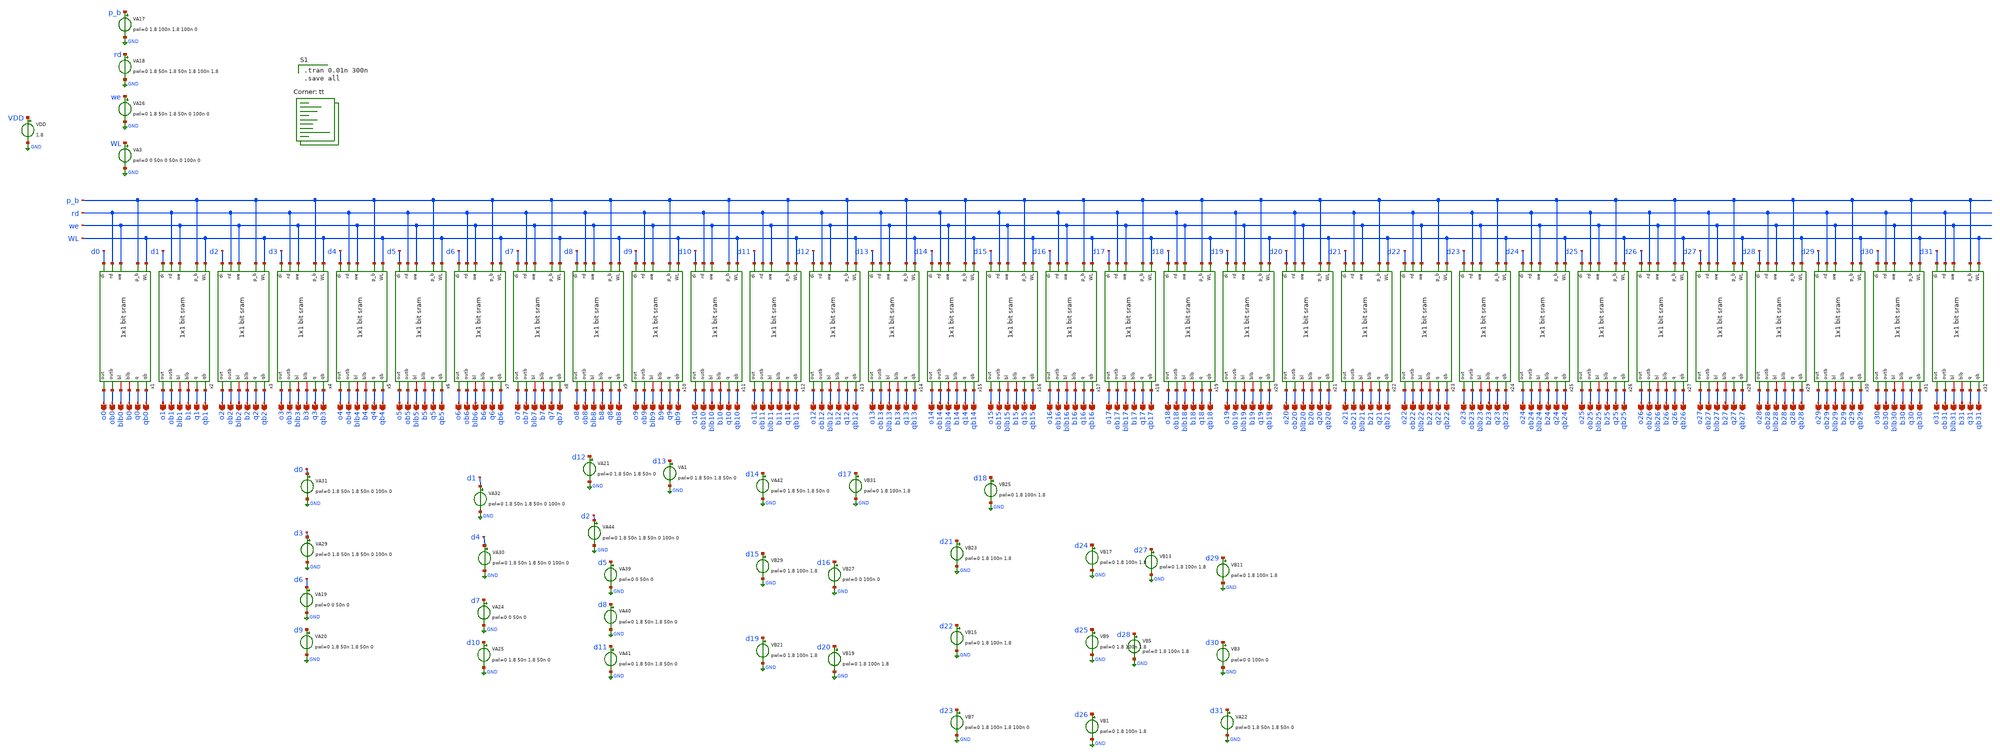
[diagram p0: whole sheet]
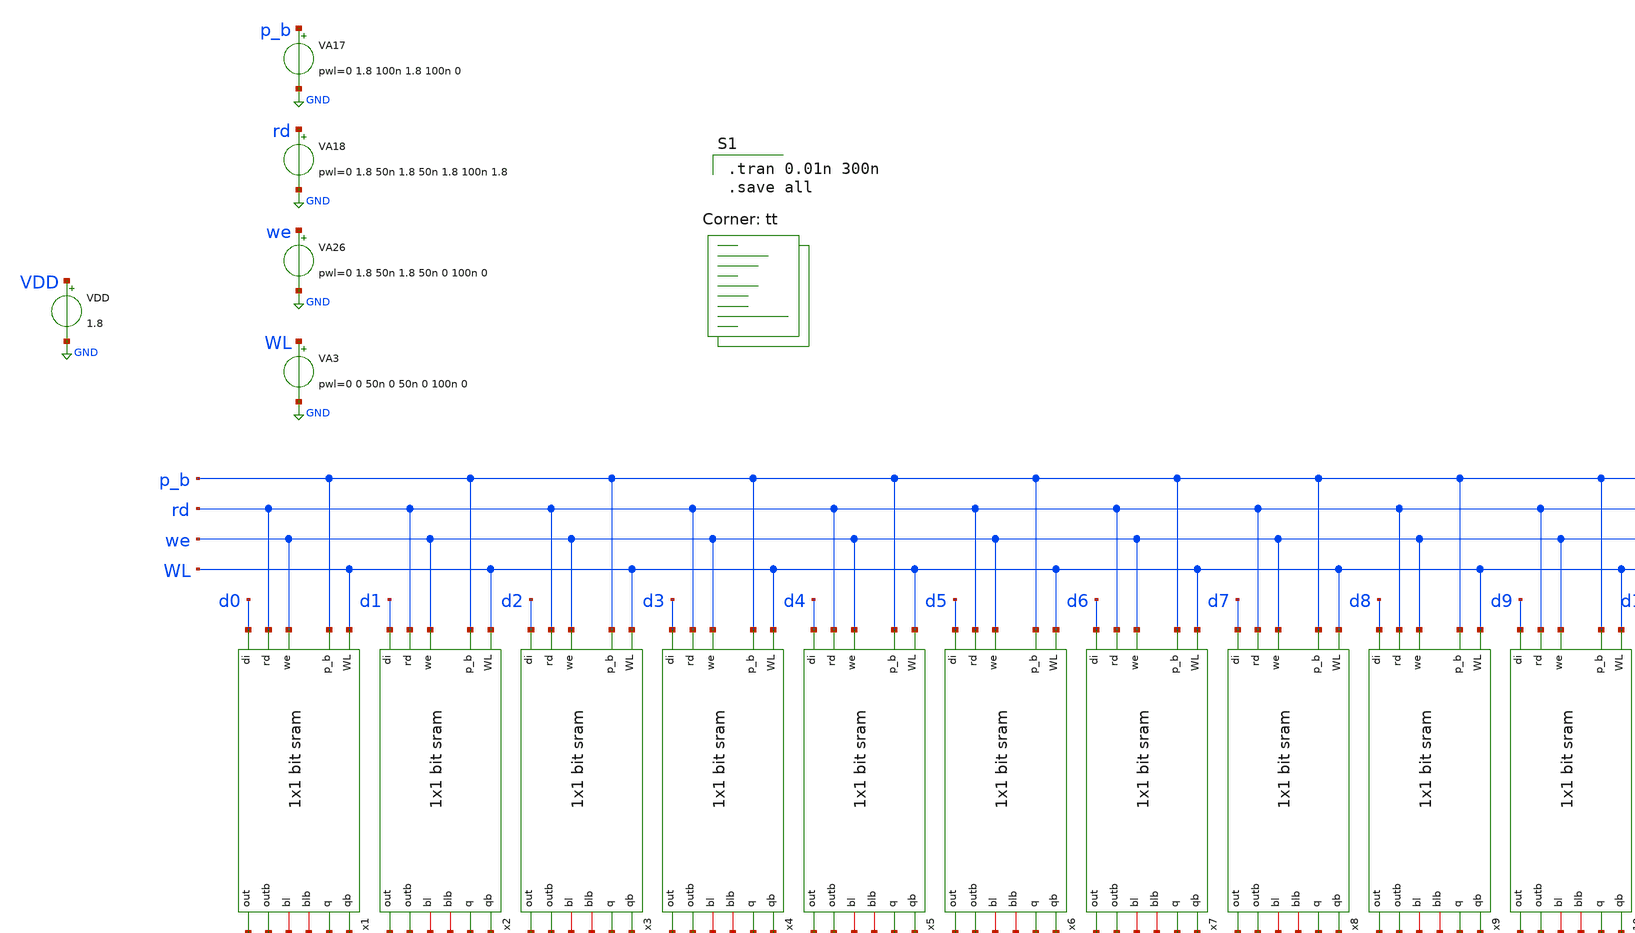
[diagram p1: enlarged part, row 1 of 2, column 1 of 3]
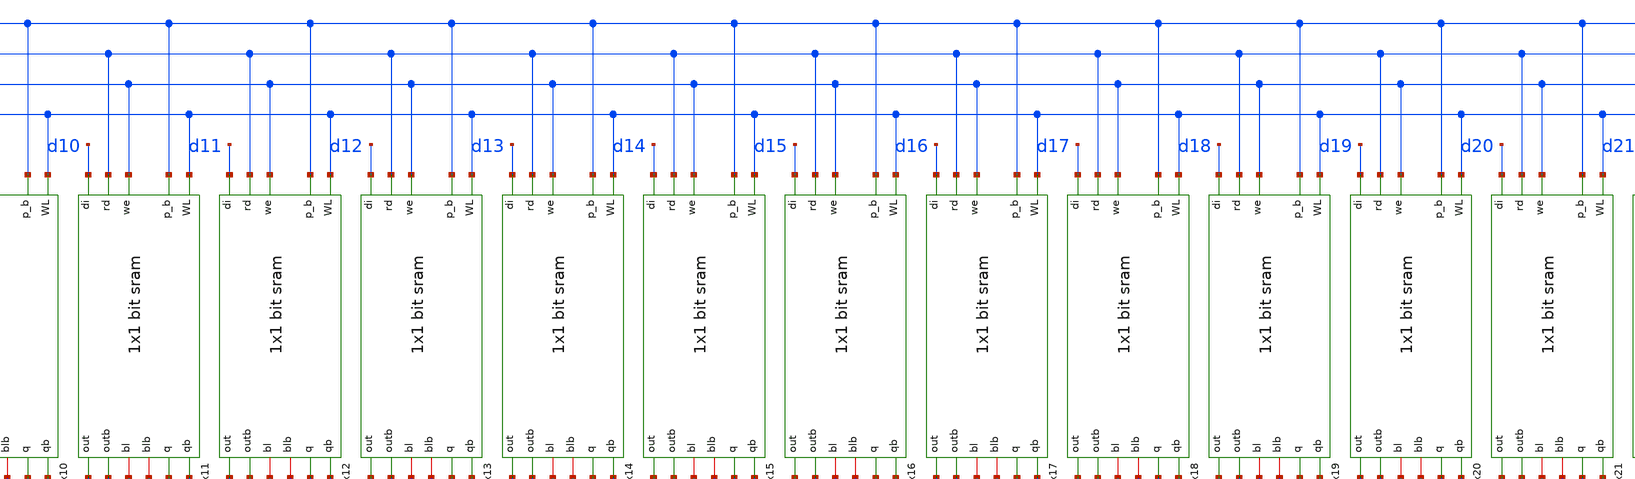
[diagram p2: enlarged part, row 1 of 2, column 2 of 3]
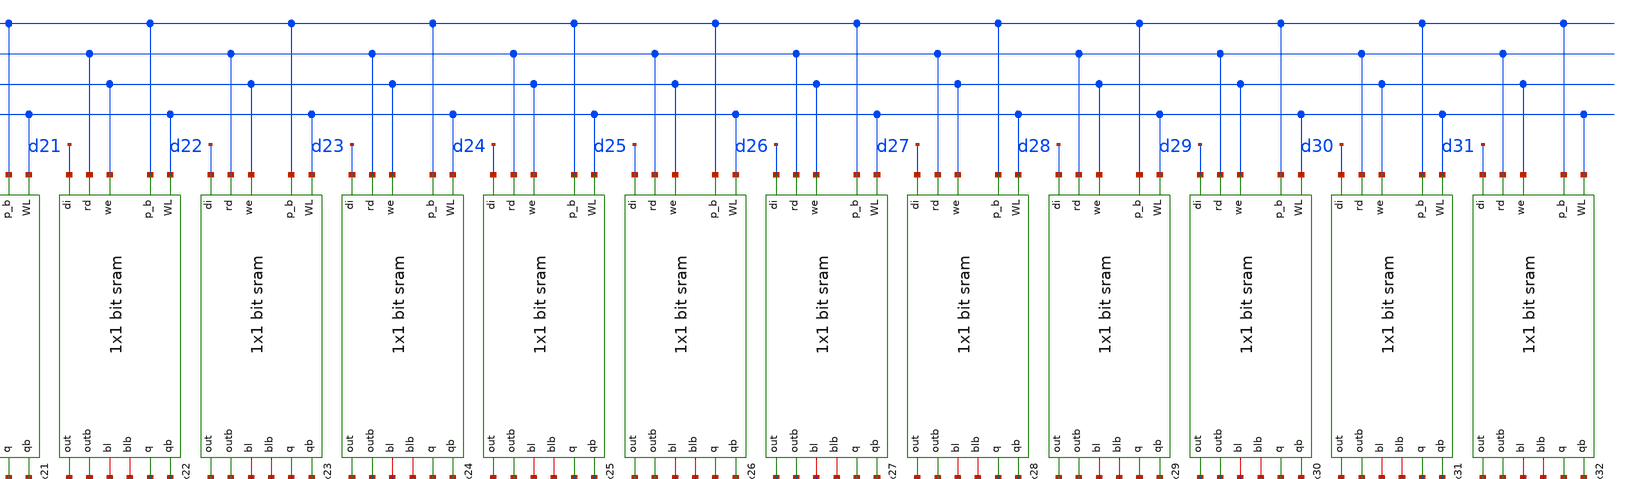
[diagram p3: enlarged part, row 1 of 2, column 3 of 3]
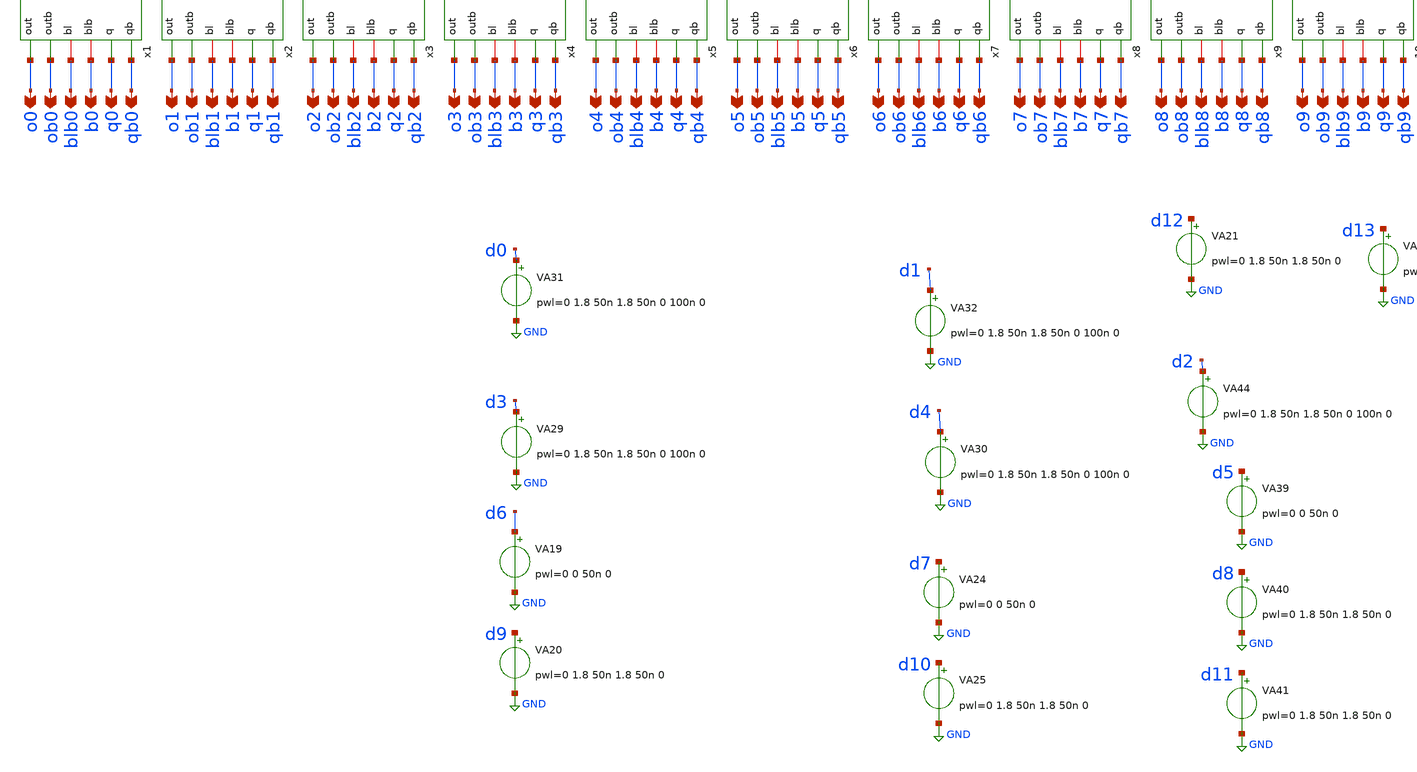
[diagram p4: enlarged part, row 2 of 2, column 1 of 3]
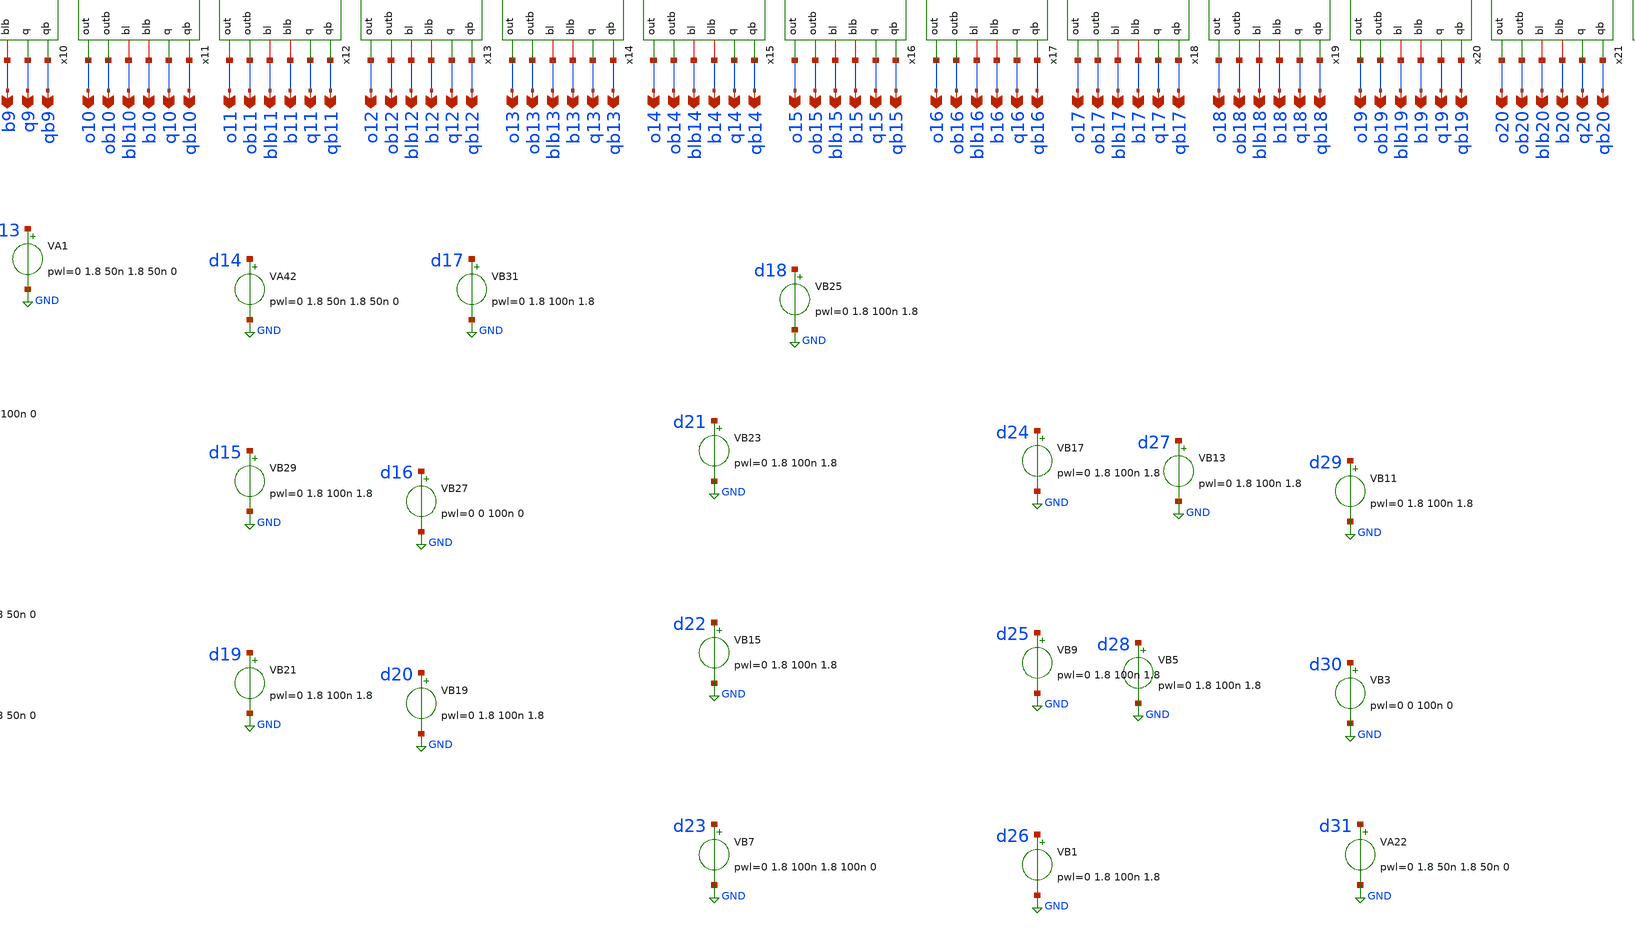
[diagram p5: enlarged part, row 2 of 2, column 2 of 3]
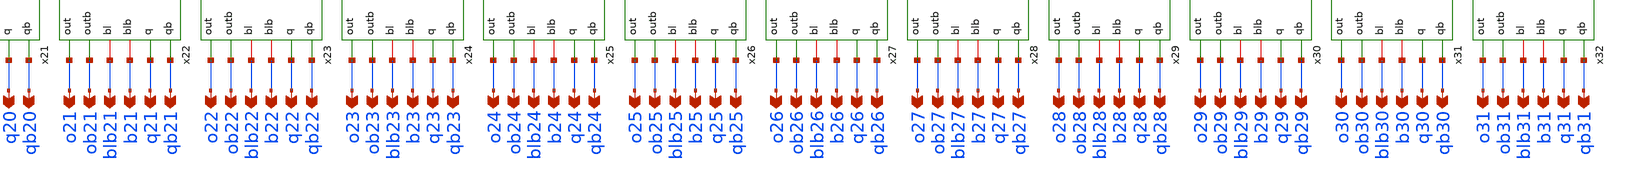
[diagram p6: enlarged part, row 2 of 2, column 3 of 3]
** sch_path: gates/32 bit SRAMsim.sch
**.subckt 32 bit SRAMsim o0 ob0 blb0 b0 q0 qb0 o1 ob1 blb1 b1 q1 qb1 o2 ob2 blb2 b2 q2 qb2 o3 ob3
*+ blb3 b3 q3 qb3 o4 ob4 blb4 b4 q4 qb4 o5 ob5 blb5 b5 q5 qb5 o6 ob6 blb6 b6 q6 qb6 o7 ob7 blb7 b7 q7 qb7
*+ o8 ob8 blb8 b8 q8 qb8 o9 ob9 blb9 b9 q9 qb9 o10 ob10 blb10 b10 q10 qb10 o11 ob11 blb11 b11 q11 qb11
*+ o12 ob12 blb12 b12 q12 qb12 o13 ob13 blb13 b13 q13 qb13 o14 ob14 blb14 b14 q14 qb14 o15 ob15 blb15 b15
*+ q15 qb15 o16 ob16 blb16 b16 q16 qb16 o17 ob17 blb17 b17 q17 qb17 o18 ob18 blb18 b18 q18 qb18 o19 ob19
*+ blb19 b19 q19 qb19 o20 ob20 blb20 b20 q20 qb20 o21 ob21 blb21 b21 q21 qb21 o22 ob22 blb22 b22 q22 qb22
*+ o23 ob23 blb23 b23 q23 qb23 o24 ob24 blb24 b24 q24 qb24 o25 ob25 blb25 b25 q25 qb25 o26 ob26 blb26 b26
*+ q26 qb26 o27 ob27 blb27 b27 q27 qb27 o28 ob28 blb28 b28 q28 qb28 o29 ob29 blb29 b29 q29 qb29 o30 ob30
*+ blb30 b30 q30 qb30 o31 ob31 blb31 b31 q31 qb31
*.opin o0
*.opin ob0
*.opin blb0
*.opin b0
*.opin q0
*.opin qb0
*.opin o1
*.opin ob1
*.opin blb1
*.opin b1
*.opin q1
*.opin qb1
*.opin o2
*.opin ob2
*.opin blb2
*.opin b2
*.opin q2
*.opin qb2
*.opin o3
*.opin ob3
*.opin blb3
*.opin b3
*.opin q3
*.opin qb3
*.opin o4
*.opin ob4
*.opin blb4
*.opin b4
*.opin q4
*.opin qb4
*.opin o5
*.opin ob5
*.opin blb5
*.opin b5
*.opin q5
*.opin qb5
*.opin o6
*.opin ob6
*.opin blb6
*.opin b6
*.opin q6
*.opin qb6
*.opin o7
*.opin ob7
*.opin blb7
*.opin b7
*.opin q7
*.opin qb7
*.opin o8
*.opin ob8
*.opin blb8
*.opin b8
*.opin q8
*.opin qb8
*.opin o9
*.opin ob9
*.opin blb9
*.opin b9
*.opin q9
*.opin qb9
*.opin o10
*.opin ob10
*.opin blb10
*.opin b10
*.opin q10
*.opin qb10
*.opin o11
*.opin ob11
*.opin blb11
*.opin b11
*.opin q11
*.opin qb11
*.opin o12
*.opin ob12
*.opin blb12
*.opin b12
*.opin q12
*.opin qb12
*.opin o13
*.opin ob13
*.opin blb13
*.opin b13
*.opin q13
*.opin qb13
*.opin o14
*.opin ob14
*.opin blb14
*.opin b14
*.opin q14
*.opin qb14
*.opin o15
*.opin ob15
*.opin blb15
*.opin b15
*.opin q15
*.opin qb15
*.opin o16
*.opin ob16
*.opin blb16
*.opin b16
*.opin q16
*.opin qb16
*.opin o17
*.opin ob17
*.opin blb17
*.opin b17
*.opin q17
*.opin qb17
*.opin o18
*.opin ob18
*.opin blb18
*.opin b18
*.opin q18
*.opin qb18
*.opin o19
*.opin ob19
*.opin blb19
*.opin b19
*.opin q19
*.opin qb19
*.opin o20
*.opin ob20
*.opin blb20
*.opin b20
*.opin q20
*.opin qb20
*.opin o21
*.opin ob21
*.opin blb21
*.opin b21
*.opin q21
*.opin qb21
*.opin o22
*.opin ob22
*.opin blb22
*.opin b22
*.opin q22
*.opin qb22
*.opin o23
*.opin ob23
*.opin blb23
*.opin b23
*.opin q23
*.opin qb23
*.opin o24
*.opin ob24
*.opin blb24
*.opin b24
*.opin q24
*.opin qb24
*.opin o25
*.opin ob25
*.opin blb25
*.opin b25
*.opin q25
*.opin qb25
*.opin o26
*.opin ob26
*.opin blb26
*.opin b26
*.opin q26
*.opin qb26
*.opin o27
*.opin ob27
*.opin blb27
*.opin b27
*.opin q27
*.opin qb27
*.opin o28
*.opin ob28
*.opin blb28
*.opin b28
*.opin q28
*.opin qb28
*.opin o29
*.opin ob29
*.opin blb29
*.opin b29
*.opin q29
*.opin qb29
*.opin o30
*.opin ob30
*.opin blb30
*.opin b30
*.opin q30
*.opin qb30
*.opin o31
*.opin ob31
*.opin blb31
*.opin b31
*.opin q31
*.opin qb31
x1 WL qb0 q0 b0 blb0 p_b we rd ob0 o0 d0 1x1 bit sram
x2 WL qb1 q1 b1 blb1 p_b we rd ob1 o1 d1 1x1 bit sram
x3 WL qb2 q2 b2 blb2 p_b we rd ob2 o2 d2 1x1 bit sram
x4 WL qb3 q3 b3 blb3 p_b we rd ob3 o3 d3 1x1 bit sram
x5 WL qb4 q4 b4 blb4 p_b we rd ob4 o4 d4 1x1 bit sram
x6 WL qb5 q5 b5 blb5 p_b we rd ob5 o5 d5 1x1 bit sram
x7 WL qb6 q6 b6 blb6 p_b we rd ob6 o6 d6 1x1 bit sram
x8 WL qb7 q7 b7 blb7 p_b we rd ob7 o7 d7 1x1 bit sram
x9 WL qb8 q8 b8 blb8 p_b we rd ob8 o8 d8 1x1 bit sram
x10 WL qb9 q9 b9 blb9 p_b we rd ob9 o9 d9 1x1 bit sram
x11 WL qb10 q10 b10 blb10 p_b we rd ob10 o10 d10 1x1 bit sram
x12 WL qb11 q11 b11 blb11 p_b we rd ob11 o11 d11 1x1 bit sram
x13 WL qb12 q12 b12 blb12 p_b we rd ob12 o12 d12 1x1 bit sram
x14 WL qb13 q13 b13 blb13 p_b we rd ob13 o13 d13 1x1 bit sram
x15 WL qb14 q14 b14 blb14 p_b we rd ob14 o14 d14 1x1 bit sram
x16 WL qb15 q15 b15 blb15 p_b we rd ob15 o15 d15 1x1 bit sram
x17 WL qb16 q16 b16 blb16 p_b we rd ob16 o16 d16 1x1 bit sram
x18 WL qb17 q17 b17 blb17 p_b we rd ob17 o17 d17 1x1 bit sram
x19 WL qb18 q18 b18 blb18 p_b we rd ob18 o18 d18 1x1 bit sram
x20 WL qb19 q19 b19 blb19 p_b we rd ob19 o19 d19 1x1 bit sram
x21 WL qb20 q20 b20 blb20 p_b we rd ob20 o20 d20 1x1 bit sram
x22 WL qb21 q21 b21 blb21 p_b we rd ob21 o21 d21 1x1 bit sram
x23 WL qb22 q22 b22 blb22 p_b we rd ob22 o22 d22 1x1 bit sram
x24 WL qb23 q23 b23 blb23 p_b we rd ob23 o23 d23 1x1 bit sram
x25 WL qb24 q24 b24 blb24 p_b we rd ob24 o24 d24 1x1 bit sram
x26 WL qb25 q25 b25 blb25 p_b we rd ob25 o25 d25 1x1 bit sram
x27 WL qb26 q26 b26 blb26 p_b we rd ob26 o26 d26 1x1 bit sram
x28 WL qb27 q27 b27 blb27 p_b we rd ob27 o27 d27 1x1 bit sram
x29 WL qb28 q28 b28 blb28 p_b we rd ob28 o28 d28 1x1 bit sram
x30 WL qb29 q29 b29 blb29 p_b we rd ob29 o29 d29 1x1 bit sram
x31 WL qb30 q30 b30 blb30 p_b we rd ob30 o30 d30 1x1 bit sram
x32 WL qb31 q31 b31 blb31 p_b we rd ob31 o31 d31 1x1 bit sram
VB1 d26 GND pwl=0 1.8 100n 1.8
VB3 d30 GND pwl=0 0 100n 0
VB5 d28 GND pwl=0 1.8 100n 1.8
VB7 d23 GND pwl=0 1.8 100n 1.8 100n 0
VB9 d25 GND pwl=0 1.8 100n 1.8
VB11 d29 GND pwl=0 1.8 100n 1.8
VB13 d27 GND pwl=0 1.8 100n 1.8
VB15 d22 GND pwl=0 1.8 100n 1.8
VB17 d24 GND pwl=0 1.8 100n 1.8
VB19 d20 GND pwl=0 1.8 100n 1.8
VB21 d19 GND pwl=0 1.8 100n 1.8
VB23 d21 GND pwl=0 1.8 100n 1.8
VB25 d18 GND pwl=0 1.8 100n 1.8
VB27 d16 GND pwl=0 0 100n 0
VB29 d15 GND pwl=0 1.8 100n 1.8
VB31 d17 GND pwl=0 1.8 100n 1.8
VA19 d6 GND pwl=0 0 50n 0
VA20 d9 GND pwl=0 1.8 50n 1.8 50n 0
VA21 d12 GND pwl=0 1.8 50n 1.8 50n 0
VA22 d31 GND pwl=0 1.8 50n 1.8 50n 0
VA24 d7 GND pwl=0 0 50n 0
VA25 d10 GND pwl=0 1.8 50n 1.8 50n 0
VA29 d3 GND pwl=0 1.8 50n 1.8 50n 0 100n 0
VA30 d4 GND pwl=0 1.8 50n 1.8 50n 0 100n 0
VA31 d0 GND pwl=0 1.8 50n 1.8 50n 0 100n 0
VA32 d1 GND pwl=0 1.8 50n 1.8 50n 0 100n 0
VA39 d5 GND pwl=0 0 50n 0
VA40 d8 GND pwl=0 1.8 50n 1.8 50n 0
VA41 d11 GND pwl=0 1.8 50n 1.8 50n 0
VA42 d14 GND pwl=0 1.8 50n 1.8 50n 0
VA44 d2 GND pwl=0 1.8 50n 1.8 50n 0 100n 0
VA17 p_b GND pwl=0 1.8 100n 1.8 100n 0
VA18 rd GND pwl=0 1.8 50n 1.8 50n 1.8 100n 1.8
VA26 we GND pwl=0 1.8 50n 1.8 50n 0 100n 0
VA3 WL GND pwl=0 0 50n 0 50n 0 100n 0
VDD VDD GND 1.8
VA1 d13 GND pwl=0 1.8 50n 1.8 50n 0
**** begin user architecture code

.tran 0.01n 300n
.save all

.lib $::SKYWATER_MODELS/sky130.lib.spice tt
**** end user architecture code
**.ends

* expanding   symbol:  Memory/1x1 bit sram.sym # of pins=11
** sym_path: gates/Memory/1x1 bit sram.sym
** sch_path: gates/Memory/1x1 bit sram.sch
.subckt 1x1 bit sram WL qb q blb bl p_b we rd outb out di
*.ipin WL
*.opin qb
*.opin q
*.ipin we
*.ipin di
*.ipin p_b
*.ipin rd
*.opin out
*.opin outb
*.iopin blb
*.iopin bl
XM1 qb q VDD VDD sky130_fd_pr__pfet_01v8 L=0.15 W=1 nf=1 ad='int((nf+1)/2) * W/nf * 0.29' as='int((nf+2)/2) * W/nf * 0.29'
+ pd='2*int((nf+1)/2) * (W/nf + 0.29)' ps='2*int((nf+2)/2) * (W/nf + 0.29)' nrd='0.29 / W' nrs='0.29 / W'
+ sa=0 sb=0 sd=0 mult=1 m=1
XM2 qb q GND GND sky130_fd_pr__nfet_01v8 L=0.15 W=1 nf=1 ad='int((nf+1)/2) * W/nf * 0.29' as='int((nf+2)/2) * W/nf * 0.29'
+ pd='2*int((nf+1)/2) * (W/nf + 0.29)' ps='2*int((nf+2)/2) * (W/nf + 0.29)' nrd='0.29 / W' nrs='0.29 / W'
+ sa=0 sb=0 sd=0 mult=1 m=1
XM3 q qb VDD VDD sky130_fd_pr__pfet_01v8 L=0.15 W=1 nf=1 ad='int((nf+1)/2) * W/nf * 0.29' as='int((nf+2)/2) * W/nf * 0.29'
+ pd='2*int((nf+1)/2) * (W/nf + 0.29)' ps='2*int((nf+2)/2) * (W/nf + 0.29)' nrd='0.29 / W' nrs='0.29 / W'
+ sa=0 sb=0 sd=0 mult=1 m=1
XM4 q qb GND GND sky130_fd_pr__nfet_01v8 L=0.15 W=1 nf=1 ad='int((nf+1)/2) * W/nf * 0.29' as='int((nf+2)/2) * W/nf * 0.29'
+ pd='2*int((nf+1)/2) * (W/nf + 0.29)' ps='2*int((nf+2)/2) * (W/nf + 0.29)' nrd='0.29 / W' nrs='0.29 / W'
+ sa=0 sb=0 sd=0 mult=1 m=1
XM5 bl WL q GND sky130_fd_pr__nfet_01v8 L=0.15 W=1 nf=1 ad='int((nf+1)/2) * W/nf * 0.29' as='int((nf+2)/2) * W/nf * 0.29'
+ pd='2*int((nf+1)/2) * (W/nf + 0.29)' ps='2*int((nf+2)/2) * (W/nf + 0.29)' nrd='0.29 / W' nrs='0.29 / W'
+ sa=0 sb=0 sd=0 mult=1 m=1
XM6 qb WL blb GND sky130_fd_pr__nfet_01v8 L=0.15 W=1 nf=1 ad='int((nf+1)/2) * W/nf * 0.29' as='int((nf+2)/2) * W/nf * 0.29'
+ pd='2*int((nf+1)/2) * (W/nf + 0.29)' ps='2*int((nf+2)/2) * (W/nf + 0.29)' nrd='0.29 / W' nrs='0.29 / W'
+ sa=0 sb=0 sd=0 mult=1 m=1
X1 we net7 inv_vtc
X5 di net3 inv_vtc
XM7 net5 net7 VDD VDD sky130_fd_pr__pfet_01v8 L=0.15 W=1 nf=1 ad='int((nf+1)/2) * W/nf * 0.29' as='int((nf+2)/2) * W/nf * 0.29'
+ pd='2*int((nf+1)/2) * (W/nf + 0.29)' ps='2*int((nf+2)/2) * (W/nf + 0.29)' nrd='0.29 / W' nrs='0.29 / W'
+ sa=0 sb=0 sd=0 mult=1 m=1
XM8 blb di net5 VDD sky130_fd_pr__pfet_01v8 L=0.15 W=1 nf=1 ad='int((nf+1)/2) * W/nf * 0.29' as='int((nf+2)/2) * W/nf * 0.29'
+ pd='2*int((nf+1)/2) * (W/nf + 0.29)' ps='2*int((nf+2)/2) * (W/nf + 0.29)' nrd='0.29 / W' nrs='0.29 / W'
+ sa=0 sb=0 sd=0 mult=1 m=1
XM9 blb di net6 GND sky130_fd_pr__nfet_01v8 L=0.15 W=1 nf=1 ad='int((nf+1)/2) * W/nf * 0.29' as='int((nf+2)/2) * W/nf * 0.29'
+ pd='2*int((nf+1)/2) * (W/nf + 0.29)' ps='2*int((nf+2)/2) * (W/nf + 0.29)' nrd='0.29 / W' nrs='0.29 / W'
+ sa=0 sb=0 sd=0 mult=1 m=1
XM10 net6 we GND GND sky130_fd_pr__nfet_01v8 L=0.15 W=1 nf=1 ad='int((nf+1)/2) * W/nf * 0.29' as='int((nf+2)/2) * W/nf * 0.29'
+ pd='2*int((nf+1)/2) * (W/nf + 0.29)' ps='2*int((nf+2)/2) * (W/nf + 0.29)' nrd='0.29 / W' nrs='0.29 / W'
+ sa=0 sb=0 sd=0 mult=1 m=1
XM11 net1 net7 VDD VDD sky130_fd_pr__pfet_01v8 L=0.15 W=1 nf=1 ad='int((nf+1)/2) * W/nf * 0.29' as='int((nf+2)/2) * W/nf * 0.29'
+ pd='2*int((nf+1)/2) * (W/nf + 0.29)' ps='2*int((nf+2)/2) * (W/nf + 0.29)' nrd='0.29 / W' nrs='0.29 / W'
+ sa=0 sb=0 sd=0 mult=1 m=1
XM12 bl net3 net1 VDD sky130_fd_pr__pfet_01v8 L=0.15 W=1 nf=1 ad='int((nf+1)/2) * W/nf * 0.29' as='int((nf+2)/2) * W/nf * 0.29'
+ pd='2*int((nf+1)/2) * (W/nf + 0.29)' ps='2*int((nf+2)/2) * (W/nf + 0.29)' nrd='0.29 / W' nrs='0.29 / W'
+ sa=0 sb=0 sd=0 mult=1 m=1
XM13 bl net3 net2 GND sky130_fd_pr__nfet_01v8 L=0.15 W=1 nf=1 ad='int((nf+1)/2) * W/nf * 0.29' as='int((nf+2)/2) * W/nf * 0.29'
+ pd='2*int((nf+1)/2) * (W/nf + 0.29)' ps='2*int((nf+2)/2) * (W/nf + 0.29)' nrd='0.29 / W' nrs='0.29 / W'
+ sa=0 sb=0 sd=0 mult=1 m=1
XM14 net2 we GND GND sky130_fd_pr__nfet_01v8 L=0.15 W=1 nf=1 ad='int((nf+1)/2) * W/nf * 0.29' as='int((nf+2)/2) * W/nf * 0.29'
+ pd='2*int((nf+1)/2) * (W/nf + 0.29)' ps='2*int((nf+2)/2) * (W/nf + 0.29)' nrd='0.29 / W' nrs='0.29 / W'
+ sa=0 sb=0 sd=0 mult=1 m=1
XM15 bl p_b VDD VDD sky130_fd_pr__pfet_01v8 L=0.15 W=1 nf=1 ad='int((nf+1)/2) * W/nf * 0.29' as='int((nf+2)/2) * W/nf * 0.29'
+ pd='2*int((nf+1)/2) * (W/nf + 0.29)' ps='2*int((nf+2)/2) * (W/nf + 0.29)' nrd='0.29 / W' nrs='0.29 / W'
+ sa=0 sb=0 sd=0 mult=1 m=1
XM16 blb p_b bl VDD sky130_fd_pr__pfet_01v8 L=0.15 W=1 nf=1 ad='int((nf+1)/2) * W/nf * 0.29' as='int((nf+2)/2) * W/nf * 0.29'
+ pd='2*int((nf+1)/2) * (W/nf + 0.29)' ps='2*int((nf+2)/2) * (W/nf + 0.29)' nrd='0.29 / W' nrs='0.29 / W'
+ sa=0 sb=0 sd=0 mult=1 m=1
XM17 blb p_b VDD VDD sky130_fd_pr__pfet_01v8 L=0.15 W=1 nf=1 ad='int((nf+1)/2) * W/nf * 0.29' as='int((nf+2)/2) * W/nf * 0.29'
+ pd='2*int((nf+1)/2) * (W/nf + 0.29)' ps='2*int((nf+2)/2) * (W/nf + 0.29)' nrd='0.29 / W' nrs='0.29 / W'
+ sa=0 sb=0 sd=0 mult=1 m=1
XM18 out p_b VDD VDD sky130_fd_pr__pfet_01v8 L=0.15 W=1 nf=1 ad='int((nf+1)/2) * W/nf * 0.29' as='int((nf+2)/2) * W/nf * 0.29'
+ pd='2*int((nf+1)/2) * (W/nf + 0.29)' ps='2*int((nf+2)/2) * (W/nf + 0.29)' nrd='0.29 / W' nrs='0.29 / W'
+ sa=0 sb=0 sd=0 mult=1 m=1
XM19 outb p_b out VDD sky130_fd_pr__pfet_01v8 L=0.15 W=1 nf=1 ad='int((nf+1)/2) * W/nf * 0.29' as='int((nf+2)/2) * W/nf * 0.29'
+ pd='2*int((nf+1)/2) * (W/nf + 0.29)' ps='2*int((nf+2)/2) * (W/nf + 0.29)' nrd='0.29 / W' nrs='0.29 / W'
+ sa=0 sb=0 sd=0 mult=1 m=1
XM20 outb p_b VDD VDD sky130_fd_pr__pfet_01v8 L=0.15 W=1 nf=1 ad='int((nf+1)/2) * W/nf * 0.29' as='int((nf+2)/2) * W/nf * 0.29'
+ pd='2*int((nf+1)/2) * (W/nf + 0.29)' ps='2*int((nf+2)/2) * (W/nf + 0.29)' nrd='0.29 / W' nrs='0.29 / W'
+ sa=0 sb=0 sd=0 mult=1 m=1
XM21 out outb VDD VDD sky130_fd_pr__pfet_01v8 L=0.15 W=1 nf=1 ad='int((nf+1)/2) * W/nf * 0.29' as='int((nf+2)/2) * W/nf * 0.29'
+ pd='2*int((nf+1)/2) * (W/nf + 0.29)' ps='2*int((nf+2)/2) * (W/nf + 0.29)' nrd='0.29 / W' nrs='0.29 / W'
+ sa=0 sb=0 sd=0 mult=1 m=1
XM22 outb out VDD VDD sky130_fd_pr__pfet_01v8 L=0.15 W=1 nf=1 ad='int((nf+1)/2) * W/nf * 0.29' as='int((nf+2)/2) * W/nf * 0.29'
+ pd='2*int((nf+1)/2) * (W/nf + 0.29)' ps='2*int((nf+2)/2) * (W/nf + 0.29)' nrd='0.29 / W' nrs='0.29 / W'
+ sa=0 sb=0 sd=0 mult=1 m=1
XM23 outb out net4 GND sky130_fd_pr__nfet_01v8 L=0.15 W=1 nf=1 ad='int((nf+1)/2) * W/nf * 0.29' as='int((nf+2)/2) * W/nf * 0.29'
+ pd='2*int((nf+1)/2) * (W/nf + 0.29)' ps='2*int((nf+2)/2) * (W/nf + 0.29)' nrd='0.29 / W' nrs='0.29 / W'
+ sa=0 sb=0 sd=0 mult=1 m=1
XM24 out outb net4 GND sky130_fd_pr__nfet_01v8 L=0.15 W=1 nf=1 ad='int((nf+1)/2) * W/nf * 0.29' as='int((nf+2)/2) * W/nf * 0.29'
+ pd='2*int((nf+1)/2) * (W/nf + 0.29)' ps='2*int((nf+2)/2) * (W/nf + 0.29)' nrd='0.29 / W' nrs='0.29 / W'
+ sa=0 sb=0 sd=0 mult=1 m=1
XM25 net4 VDD GND GND sky130_fd_pr__nfet_01v8 L=0.15 W=1 nf=1 ad='int((nf+1)/2) * W/nf * 0.29' as='int((nf+2)/2) * W/nf * 0.29'
+ pd='2*int((nf+1)/2) * (W/nf + 0.29)' ps='2*int((nf+2)/2) * (W/nf + 0.29)' nrd='0.29 / W' nrs='0.29 / W'
+ sa=0 sb=0 sd=0 mult=1 m=1
XM26 bl rd out VDD sky130_fd_pr__pfet_01v8 L=0.15 W=1 nf=1 ad='int((nf+1)/2) * W/nf * 0.29' as='int((nf+2)/2) * W/nf * 0.29'
+ pd='2*int((nf+1)/2) * (W/nf + 0.29)' ps='2*int((nf+2)/2) * (W/nf + 0.29)' nrd='0.29 / W' nrs='0.29 / W'
+ sa=0 sb=0 sd=0 mult=1 m=1
XM27 outb rd blb VDD sky130_fd_pr__pfet_01v8 L=0.15 W=1 nf=1 ad='int((nf+1)/2) * W/nf * 0.29' as='int((nf+2)/2) * W/nf * 0.29'
+ pd='2*int((nf+1)/2) * (W/nf + 0.29)' ps='2*int((nf+2)/2) * (W/nf + 0.29)' nrd='0.29 / W' nrs='0.29 / W'
+ sa=0 sb=0 sd=0 mult=1 m=1
.ends


* expanding   symbol:  /home/apn/test_xschem_sky130/inv_vtc.sym # of pins=2
** sym_path: gates/inv_vtc.sym
** sch_path: gates/inv_vtc.sch
.subckt inv_vtc A Y
*.ipin A
*.opin Y
XM1 Y A VDD VDD sky130_fd_pr__pfet_01v8 L=0.15 W=2 nf=1 ad='int((nf+1)/2) * W/nf * 0.29' as='int((nf+2)/2) * W/nf * 0.29'
+ pd='2*int((nf+1)/2) * (W/nf + 0.29)' ps='2*int((nf+2)/2) * (W/nf + 0.29)' nrd='0.29 / W' nrs='0.29 / W'
+ sa=0 sb=0 sd=0 mult=1 m=1
XM2 Y A GND GND sky130_fd_pr__nfet_01v8 L=0.15 W=1 nf=1 ad='int((nf+1)/2) * W/nf * 0.29' as='int((nf+2)/2) * W/nf * 0.29'
+ pd='2*int((nf+1)/2) * (W/nf + 0.29)' ps='2*int((nf+2)/2) * (W/nf + 0.29)' nrd='0.29 / W' nrs='0.29 / W'
+ sa=0 sb=0 sd=0 mult=1 m=1
.ends

.GLOBAL GND
.GLOBAL VDD
.end
